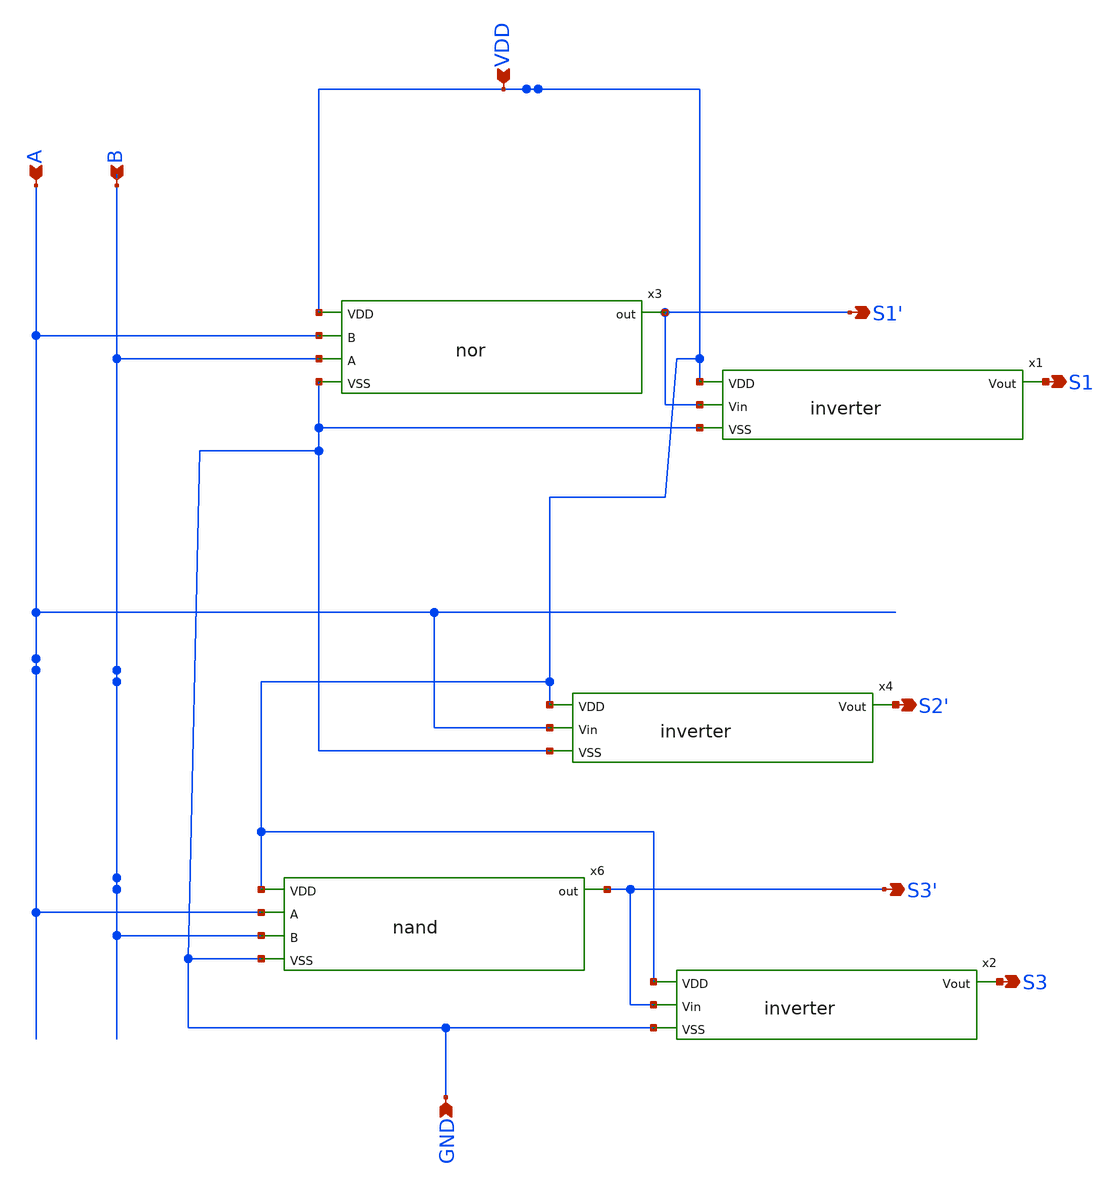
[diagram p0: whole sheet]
** sch_path: 2_bit_current_steering_DAC/decoder.sch
**.subckt decoder A B VDD GND S1' S1 S2' S3 S3'
*.ipin A
*.ipin B
*.ipin VDD
*.ipin GND
*.opin S1'
*.opin S1
*.opin S2'
*.opin S3
*.opin S3'
x3 VDD A S1' B GND nor
x1 VDD S1' S1 GND inverter
x4 VDD A S2' GND inverter
x6 VDD A S3' B GND nand
x2 VDD S3' S3 GND inverter
**.ends

* expanding   symbol:  nor.sym # of pins=5
** sym_path: 2_bit_current_steering_DAC/nor.sym
** sch_path: 2_bit_current_steering_DAC/nor.sch
.subckt nor VDD B out A VSS
*.ipin A
*.ipin B
*.ipin VDD
*.ipin VSS
*.opin out
XM1 out A VSS GND sky130_fd_pr__nfet_01v8 L=0.15 W=1 nf=1 ad='int((1 + 1)/2) * 1 / 1 * 0.29' as='int((1
+ + 2)/2) * 1 / 1 * 0.29' pd='2*int((1 + 1)/2) * (1 / 1 + 0.29)' ps='2*int((1 + 2)/2) * (1 / 1 + 0.29)' nrd='0.29
+ / 1 ' nrs='0.29 / 1 ' sa=0 sb=0 sd=0 mult=1 m=1
XM3 out B VSS GND sky130_fd_pr__nfet_01v8 L=0.15 W=1 nf=1 ad='int((1 + 1)/2) * 1 / 1 * 0.29' as='int((1
+ + 2)/2) * 1 / 1 * 0.29' pd='2*int((1 + 1)/2) * (1 / 1 + 0.29)' ps='2*int((1 + 2)/2) * (1 / 1 + 0.29)' nrd='0.29
+ / 1 ' nrs='0.29 / 1 ' sa=0 sb=0 sd=0 mult=1 m=1
XM2 out A net1 VDD sky130_fd_pr__pfet_01v8 L=0.15 W=1 nf=1 ad='int((1 + 1)/2) * 1 / 1 * 0.29' as='int((1
+ + 2)/2) * 1 / 1 * 0.29' pd='2*int((1 + 1)/2) * (1 / 1 + 0.29)' ps='2*int((1 + 2)/2) * (1 / 1 + 0.29)' nrd='0.29
+ / 1 ' nrs='0.29 / 1 ' sa=0 sb=0 sd=0 mult=1 m=1
XM4 net1 B VDD VDD sky130_fd_pr__pfet_01v8 L=0.15 W=1 nf=1 ad='int((1 + 1)/2) * 1 / 1 * 0.29' as='int((1
+ + 2)/2) * 1 / 1 * 0.29' pd='2*int((1 + 1)/2) * (1 / 1 + 0.29)' ps='2*int((1 + 2)/2) * (1 / 1 + 0.29)' nrd='0.29
+ / 1 ' nrs='0.29 / 1 ' sa=0 sb=0 sd=0 mult=1 m=1
.ends


* expanding   symbol:  inverter.sym # of pins=4
** sym_path: 2_bit_current_steering_DAC/inverter.sym
** sch_path: 2_bit_current_steering_DAC/inverter.sch
.subckt inverter VDD Vin Vout VSS
*.ipin VDD
*.ipin Vin
*.ipin VSS
*.opin Vout
XM1 Vout Vin VSS GND sky130_fd_pr__nfet_01v8 L=0.15 W=1 nf=1 ad='int((1 + 1)/2) * 1 / 1 * 0.29' as='int((1
+ + 2)/2) * 1 / 1 * 0.29' pd='2*int((1 + 1)/2) * (1 / 1 + 0.29)' ps='2*int((1 + 2)/2) * (1 / 1 + 0.29)' nrd='0.29
+ / 1 ' nrs='0.29 / 1 ' sa=0 sb=0 sd=0 mult=1 m=1
XM2 Vout Vin VDD VDD sky130_fd_pr__pfet_01v8 L=0.15 W=1 nf=1 ad='int((1 + 1)/2) * 1 / 1 * 0.29' as='int((1
+ + 2)/2) * 1 / 1 * 0.29' pd='2*int((1 + 1)/2) * (1 / 1 + 0.29)' ps='2*int((1 + 2)/2) * (1 / 1 + 0.29)' nrd='0.29
+ / 1 ' nrs='0.29 / 1 ' sa=0 sb=0 sd=0 mult=1 m=1
.ends


* expanding   symbol:  nand.sym # of pins=5
** sym_path: 2_bit_current_steering_DAC/nand.sym
** sch_path: 2_bit_current_steering_DAC/nand.sch
.subckt nand VDD A out B VSS
*.ipin A
*.ipin VDD
*.ipin B
*.ipin VSS
*.opin out
XM1 net1 B VSS GND sky130_fd_pr__nfet_01v8 L=0.15 W=1 nf=1 ad='int((1 + 1)/2) * 1 / 1 * 0.29' as='int((1
+ + 2)/2) * 1 / 1 * 0.29' pd='2*int((1 + 1)/2) * (1 / 1 + 0.29)' ps='2*int((1 + 2)/2) * (1 / 1 + 0.29)' nrd='0.29
+ / 1 ' nrs='0.29 / 1 ' sa=0 sb=0 sd=0 mult=1 m=1
XM2 out A net1 GND sky130_fd_pr__nfet_01v8 L=0.15 W=1 nf=1 ad='int((1 + 1)/2) * 1 / 1 * 0.29' as='int((1
+ + 2)/2) * 1 / 1 * 0.29' pd='2*int((1 + 1)/2) * (1 / 1 + 0.29)' ps='2*int((1 + 2)/2) * (1 / 1 + 0.29)' nrd='0.29
+ / 1 ' nrs='0.29 / 1 ' sa=0 sb=0 sd=0 mult=1 m=1
XM3 out A VDD VDD sky130_fd_pr__pfet_01v8 L=0.15 W=1 nf=1 ad='int((1 + 1)/2) * 1 / 1 * 0.29' as='int((1
+ + 2)/2) * 1 / 1 * 0.29' pd='2*int((1 + 1)/2) * (1 / 1 + 0.29)' ps='2*int((1 + 2)/2) * (1 / 1 + 0.29)' nrd='0.29
+ / 1 ' nrs='0.29 / 1 ' sa=0 sb=0 sd=0 mult=1 m=1
XM4 out B VDD VDD sky130_fd_pr__pfet_01v8 L=0.15 W=1 nf=1 ad='int((1 + 1)/2) * 1 / 1 * 0.29' as='int((1
+ + 2)/2) * 1 / 1 * 0.29' pd='2*int((1 + 1)/2) * (1 / 1 + 0.29)' ps='2*int((1 + 2)/2) * (1 / 1 + 0.29)' nrd='0.29
+ / 1 ' nrs='0.29 / 1 ' sa=0 sb=0 sd=0 mult=1 m=1
.ends

.end
